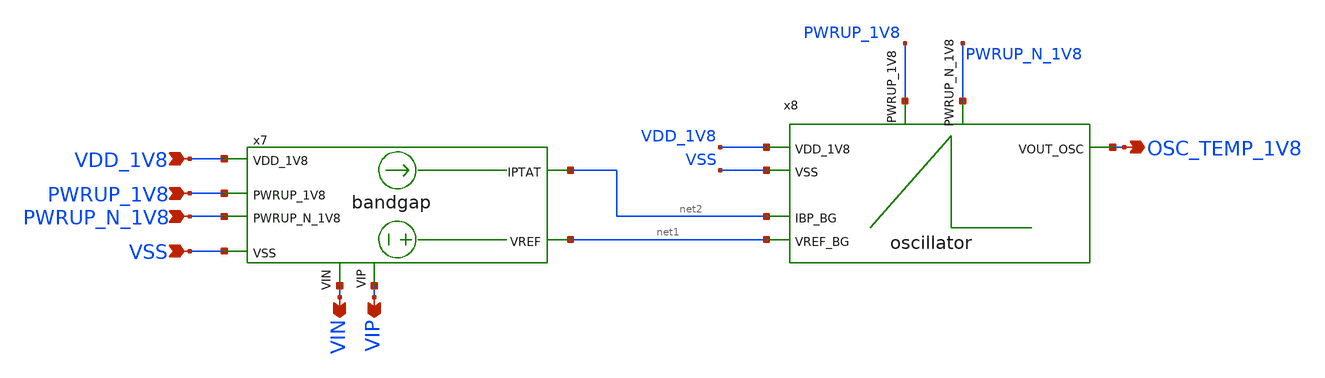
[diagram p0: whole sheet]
** sch_path: design/LELO_GR01_SKY130A/LELO_GR01.sch
**.subckt LELO_GR01 VDD_1V8 VSS PWRUP_1V8 OSC_TEMP_1V8 PWRUP_N_1V8 VIN VIP
*.ipin VDD_1V8
*.ipin VSS
*.ipin PWRUP_1V8
*.opin OSC_TEMP_1V8
*.ipin PWRUP_N_1V8
*.opin VIN
*.opin VIP
x7 net2 net1 PWRUP_1V8 VDD_1V8 VSS PWRUP_N_1V8 VIN VIP bandgap
x8 OSC_TEMP_1V8 VDD_1V8 VSS net2 net1 PWRUP_1V8 PWRUP_N_1V8 oscillator
**.ends
.end
